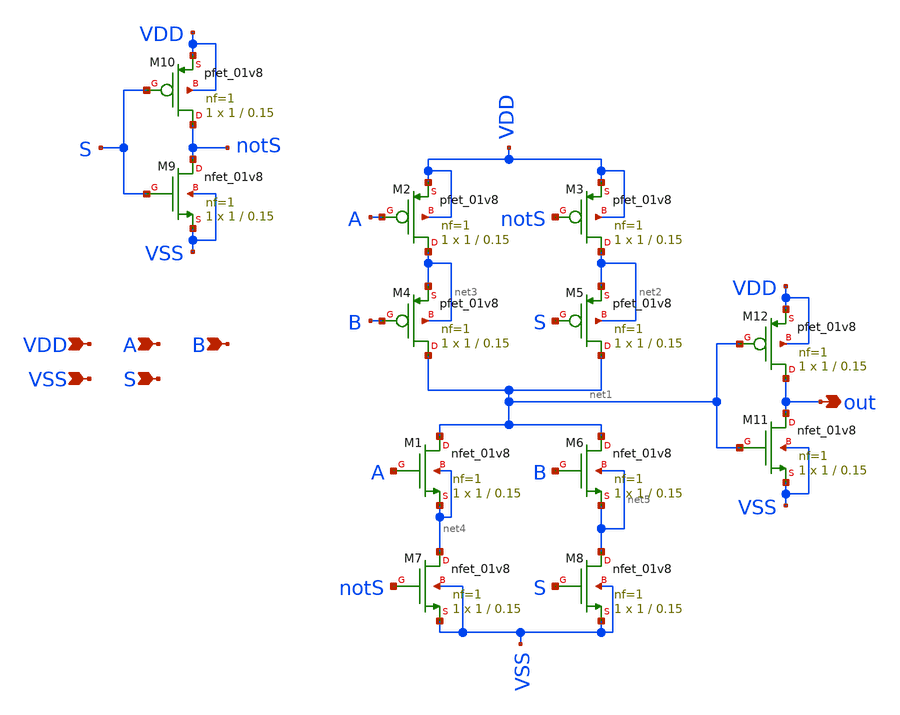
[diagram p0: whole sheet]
** sch_path: 2x1_mux/2x1_mux.sch
**.subckt 2x1_mux VDD A B out S VSS
*.ipin VDD
*.ipin A
*.ipin B
*.opin out
*.ipin S
*.ipin VSS
XM1 net1 A net4 net4 sky130_fd_pr__nfet_01v8 L=0.15 W=1 nf=1 ad='int((nf+1)/2) * W/nf * 0.29' as='int((nf+2)/2) * W/nf * 0.29'
+ pd='2*int((nf+1)/2) * (W/nf + 0.29)' ps='2*int((nf+2)/2) * (W/nf + 0.29)' nrd='0.29 / W' nrs='0.29 / W'
+ sa=0 sb=0 sd=0 mult=1 m=1
XM2 net3 A VDD VDD sky130_fd_pr__pfet_01v8 L=0.15 W=1 nf=1 ad='int((nf+1)/2) * W/nf * 0.29' as='int((nf+2)/2) * W/nf * 0.29'
+ pd='2*int((nf+1)/2) * (W/nf + 0.29)' ps='2*int((nf+2)/2) * (W/nf + 0.29)' nrd='0.29 / W' nrs='0.29 / W'
+ sa=0 sb=0 sd=0 mult=1 m=1
XM3 net2 notS VDD VDD sky130_fd_pr__pfet_01v8 L=0.15 W=1 nf=1 ad='int((nf+1)/2) * W/nf * 0.29' as='int((nf+2)/2) * W/nf * 0.29'
+ pd='2*int((nf+1)/2) * (W/nf + 0.29)' ps='2*int((nf+2)/2) * (W/nf + 0.29)' nrd='0.29 / W' nrs='0.29 / W'
+ sa=0 sb=0 sd=0 mult=1 m=1
XM4 net1 B net3 net3 sky130_fd_pr__pfet_01v8 L=0.15 W=1 nf=1 ad='int((nf+1)/2) * W/nf * 0.29' as='int((nf+2)/2) * W/nf * 0.29'
+ pd='2*int((nf+1)/2) * (W/nf + 0.29)' ps='2*int((nf+2)/2) * (W/nf + 0.29)' nrd='0.29 / W' nrs='0.29 / W'
+ sa=0 sb=0 sd=0 mult=1 m=1
XM5 net1 S net2 net2 sky130_fd_pr__pfet_01v8 L=0.15 W=1 nf=1 ad='int((nf+1)/2) * W/nf * 0.29' as='int((nf+2)/2) * W/nf * 0.29'
+ pd='2*int((nf+1)/2) * (W/nf + 0.29)' ps='2*int((nf+2)/2) * (W/nf + 0.29)' nrd='0.29 / W' nrs='0.29 / W'
+ sa=0 sb=0 sd=0 mult=1 m=1
XM6 net1 B net5 net5 sky130_fd_pr__nfet_01v8 L=0.15 W=1 nf=1 ad='int((nf+1)/2) * W/nf * 0.29' as='int((nf+2)/2) * W/nf * 0.29'
+ pd='2*int((nf+1)/2) * (W/nf + 0.29)' ps='2*int((nf+2)/2) * (W/nf + 0.29)' nrd='0.29 / W' nrs='0.29 / W'
+ sa=0 sb=0 sd=0 mult=1 m=1
XM7 net4 notS VSS VSS sky130_fd_pr__nfet_01v8 L=0.15 W=1 nf=1 ad='int((nf+1)/2) * W/nf * 0.29' as='int((nf+2)/2) * W/nf * 0.29'
+ pd='2*int((nf+1)/2) * (W/nf + 0.29)' ps='2*int((nf+2)/2) * (W/nf + 0.29)' nrd='0.29 / W' nrs='0.29 / W'
+ sa=0 sb=0 sd=0 mult=1 m=1
XM8 net5 S VSS VSS sky130_fd_pr__nfet_01v8 L=0.15 W=1 nf=1 ad='int((nf+1)/2) * W/nf * 0.29' as='int((nf+2)/2) * W/nf * 0.29'
+ pd='2*int((nf+1)/2) * (W/nf + 0.29)' ps='2*int((nf+2)/2) * (W/nf + 0.29)' nrd='0.29 / W' nrs='0.29 / W'
+ sa=0 sb=0 sd=0 mult=1 m=1
XM9 notS S VSS VSS sky130_fd_pr__nfet_01v8 L=0.15 W=1 nf=1 ad='int((nf+1)/2) * W/nf * 0.29' as='int((nf+2)/2) * W/nf * 0.29'
+ pd='2*int((nf+1)/2) * (W/nf + 0.29)' ps='2*int((nf+2)/2) * (W/nf + 0.29)' nrd='0.29 / W' nrs='0.29 / W'
+ sa=0 sb=0 sd=0 mult=1 m=1
XM10 notS S VDD VDD sky130_fd_pr__pfet_01v8 L=0.15 W=1 nf=1 ad='int((nf+1)/2) * W/nf * 0.29' as='int((nf+2)/2) * W/nf * 0.29'
+ pd='2*int((nf+1)/2) * (W/nf + 0.29)' ps='2*int((nf+2)/2) * (W/nf + 0.29)' nrd='0.29 / W' nrs='0.29 / W'
+ sa=0 sb=0 sd=0 mult=1 m=1
XM11 out net1 VSS VSS sky130_fd_pr__nfet_01v8 L=0.15 W=1 nf=1 ad='int((nf+1)/2) * W/nf * 0.29' as='int((nf+2)/2) * W/nf * 0.29'
+ pd='2*int((nf+1)/2) * (W/nf + 0.29)' ps='2*int((nf+2)/2) * (W/nf + 0.29)' nrd='0.29 / W' nrs='0.29 / W'
+ sa=0 sb=0 sd=0 mult=1 m=1
XM12 out net1 VDD VDD sky130_fd_pr__pfet_01v8 L=0.15 W=1 nf=1 ad='int((nf+1)/2) * W/nf * 0.29' as='int((nf+2)/2) * W/nf * 0.29'
+ pd='2*int((nf+1)/2) * (W/nf + 0.29)' ps='2*int((nf+2)/2) * (W/nf + 0.29)' nrd='0.29 / W' nrs='0.29 / W'
+ sa=0 sb=0 sd=0 mult=1 m=1
**.ends
.end
